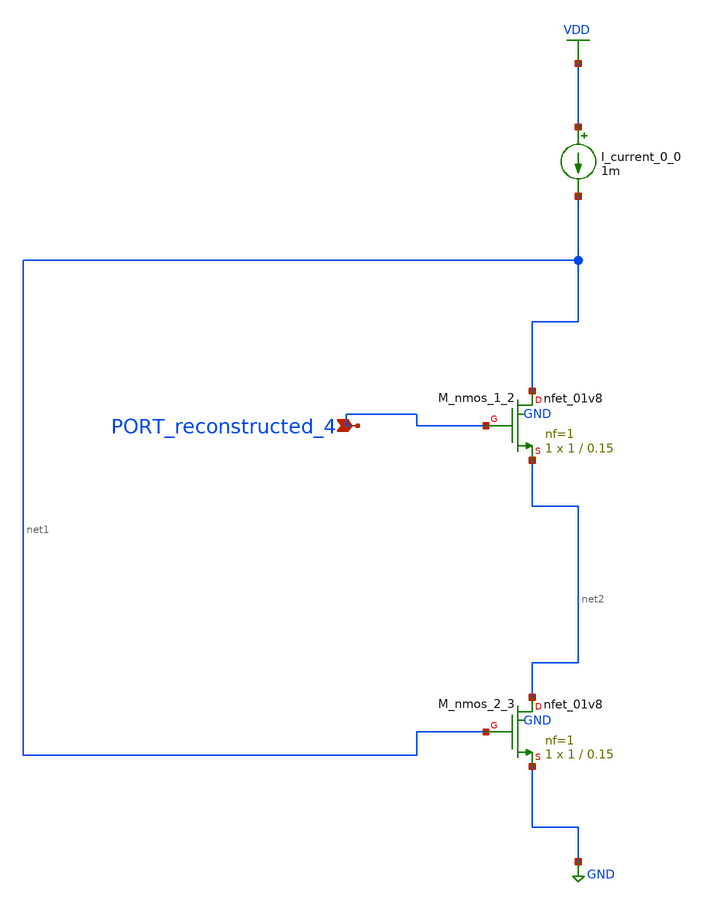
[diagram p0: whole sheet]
** sch_path: schematics/AMSNet/263.sch
**.subckt 263 PORT_reconstructed_4
*.ipin PORT_reconstructed_4
I_current_0_0 VDD net1 1m
XM_nmos_1_2 net1 PORT_reconstructed_4 net2 GND sky130_fd_pr__nfet_01v8 L=0.15 W=1 nf=1 ad='int((1 + 1)/2) * 1 / 1 * 0.29'
+ as='int((1 + 2)/2) * 1 / 1 * 0.29' pd='2*int((1 + 1)/2) * (1 / 1 + 0.29)' ps='2*int((1 + 2)/2) * (1 / 1 + 0.29)'
+ nrd='0.29 / 1 ' nrs='0.29 / 1 ' sa=0 sb=0 sd=0 mult=1 m=1
XM_nmos_2_3 net2 net1 GND GND sky130_fd_pr__nfet_01v8 L=0.15 W=1 nf=1 ad='int((1 + 1)/2) * 1 / 1 * 0.29'
+ as='int((1 + 2)/2) * 1 / 1 * 0.29' pd='2*int((1 + 1)/2) * (1 / 1 + 0.29)' ps='2*int((1 + 2)/2) * (1 / 1 + 0.29)'
+ nrd='0.29 / 1 ' nrs='0.29 / 1 ' sa=0 sb=0 sd=0 mult=1 m=1
**.ends
.GLOBAL GND
.GLOBAL VDD
.end
